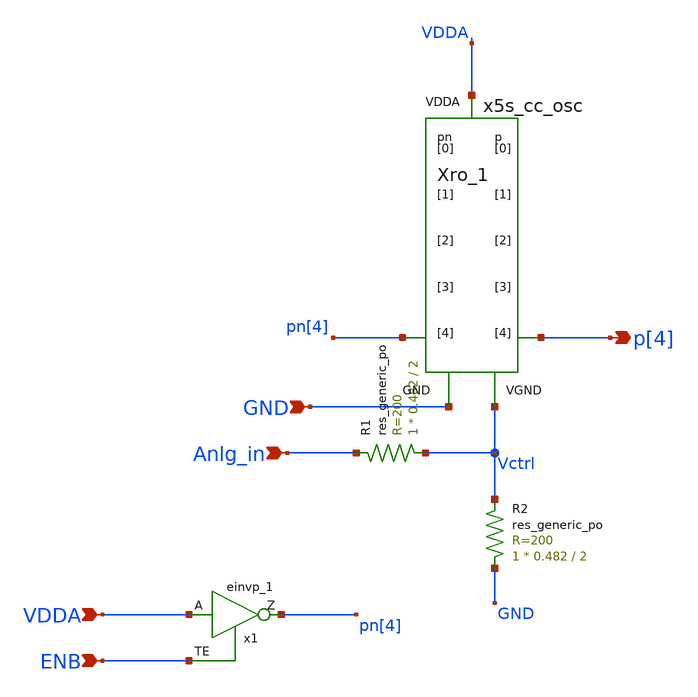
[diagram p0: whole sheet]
** sch_path: xschem/lib/ALib_VCO.sch
**.subckt ALib_VCO Anlg_in VDDA ENB p[4] GND
*.ipin Anlg_in
*.ipin VDDA
*.ipin ENB
*.opin p[4]
*.ipin GND
x1 VDDA ENB GND GND VDDA VDDA pn[4] sky130_fd_sc_hd__einvp_1
XR1 Vctrl Anlg_in sky130_fd_pr__res_generic_po W=0.482 L=2 m=1
XR2 GND Vctrl sky130_fd_pr__res_generic_po W=0.482 L=2 m=1
Xro_1 pn[4] p[4] Vctrl VDDA GND x5s_cc_osc
**.ends
.end
